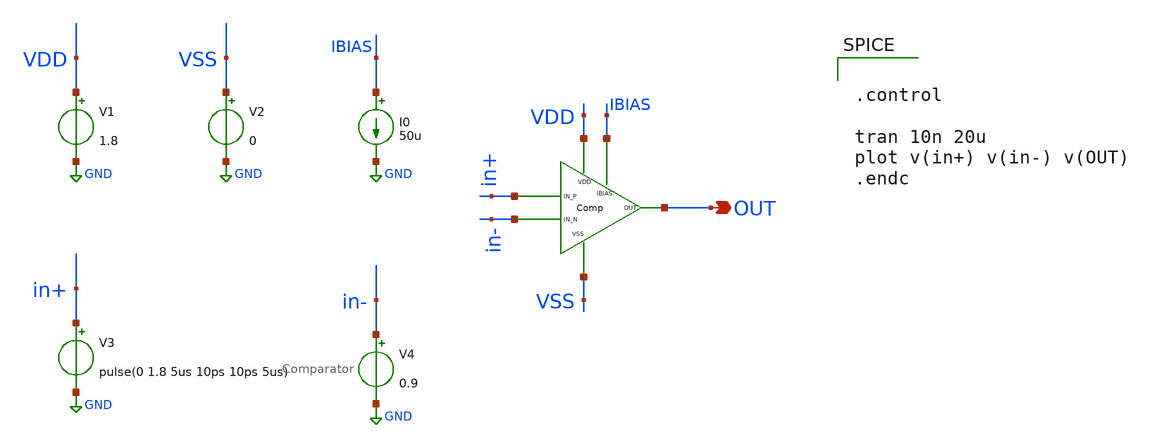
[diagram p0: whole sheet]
** sch_path: xschem/DC_DC_Converter_xschem/OTHERS/DC_DC_Converter_V7/Comparator/Comparator_TB.sch
**.subckt Comparator_TB OUT
*.opin OUT
V1 VDD GND 1.8
V2 VSS GND 0
V3 in+ GND pulse(0 1.8 5us 10ps 10ps 5us)
V4 in- GND 0.9
I0 IBIAS GND 50u
XM1 IBIAS VDD in+ in- VSS OUT Comparator
**** begin user architecture code


.control

tran 10n 20u
plot v(in+) v(in-) v(OUT)
.endc



** opencircuitdesign pdks install
.lib $::SKYWATER_MODELS/sky130.lib.spice tt


**** end user architecture code
**.ends

* expanding   symbol:  DC_DC_Converter/Comparator/Comparator.sym # of pins=6
** sym_path: xschem/DC_DC_Converter_xschem/OTHERS/DC_DC_Converter_V7/Comparator/Comparator.sym
** sch_path: xschem/DC_DC_Converter_xschem/OTHERS/DC_DC_Converter_V7/Comparator/Comparator.sch
.subckt Comparator IBIAS VDD IN_P IN_N VSS OUT
*.iopin VDD
*.iopin VSS
*.iopin IN_P
*.iopin IN_N
*.iopin OUT
*.iopin IBIAS
XM15 1_N IN_P IBIAS VSS sky130_fd_pr__nfet_01v8 L=1 W=5 nf=1 ad='int((nf+1)/2) * W/nf * 0.29' as='int((nf+2)/2) * W/nf * 0.29'
+ pd='2*int((nf+1)/2) * (W/nf + 0.29)' ps='2*int((nf+2)/2) * (W/nf + 0.29)' nrd='0.29 / W' nrs='0.29 / W'
+ sa=0 sb=0 sd=0 mult=1 m=1
XM1 1_P IN_N IBIAS VSS sky130_fd_pr__nfet_01v8 L=1 W=5 nf=1 ad='int((nf+1)/2) * W/nf * 0.29' as='int((nf+2)/2) * W/nf * 0.29'
+ pd='2*int((nf+1)/2) * (W/nf + 0.29)' ps='2*int((nf+2)/2) * (W/nf + 0.29)' nrd='0.29 / W' nrs='0.29 / W'
+ sa=0 sb=0 sd=0 mult=1 m=1
XM2 2_P 2_P VSS VSS sky130_fd_pr__nfet_01v8 L=2 W=2 nf=1 ad='int((nf+1)/2) * W/nf * 0.29' as='int((nf+2)/2) * W/nf * 0.29'
+ pd='2*int((nf+1)/2) * (W/nf + 0.29)' ps='2*int((nf+2)/2) * (W/nf + 0.29)' nrd='0.29 / W' nrs='0.29 / W'
+ sa=0 sb=0 sd=0 mult=1 m=1
XM10 2_N 2_P VSS VSS sky130_fd_pr__nfet_01v8 L=2 W=2 nf=1 ad='int((nf+1)/2) * W/nf * 0.29' as='int((nf+2)/2) * W/nf * 0.29'
+ pd='2*int((nf+1)/2) * (W/nf + 0.29)' ps='2*int((nf+2)/2) * (W/nf + 0.29)' nrd='0.29 / W' nrs='0.29 / W'
+ sa=0 sb=0 sd=0 mult=1 m=1
XM11 OP_1 2_N VSS VSS sky130_fd_pr__nfet_01v8 L=1 W=1 nf=1 ad='int((nf+1)/2) * W/nf * 0.29' as='int((nf+2)/2) * W/nf * 0.29'
+ pd='2*int((nf+1)/2) * (W/nf + 0.29)' ps='2*int((nf+2)/2) * (W/nf + 0.29)' nrd='0.29 / W' nrs='0.29 / W'
+ sa=0 sb=0 sd=0 mult=1 m=1
XM13 OUT OP_1 VSS VSS sky130_fd_pr__nfet_01v8 L=1 W=1 nf=1 ad='int((nf+1)/2) * W/nf * 0.29' as='int((nf+2)/2) * W/nf * 0.29'
+ pd='2*int((nf+1)/2) * (W/nf + 0.29)' ps='2*int((nf+2)/2) * (W/nf + 0.29)' nrd='0.29 / W' nrs='0.29 / W'
+ sa=0 sb=0 sd=0 mult=1 m=1
XM9 2_P 1_N VDD VDD sky130_fd_pr__pfet_01v8 L=0.5 W=1 nf=1 ad='int((nf+1)/2) * W/nf * 0.29' as='int((nf+2)/2) * W/nf * 0.29'
+ pd='2*int((nf+1)/2) * (W/nf + 0.29)' ps='2*int((nf+2)/2) * (W/nf + 0.29)' nrd='0.29 / W' nrs='0.29 / W'
+ sa=0 sb=0 sd=0 mult=1 m=1
XM6 1_N 1_N VDD VDD sky130_fd_pr__pfet_01v8 L=0.5 W=1.5 nf=1 ad='int((nf+1)/2) * W/nf * 0.29' as='int((nf+2)/2) * W/nf * 0.29'
+ pd='2*int((nf+1)/2) * (W/nf + 0.29)' ps='2*int((nf+2)/2) * (W/nf + 0.29)' nrd='0.29 / W' nrs='0.29 / W'
+ sa=0 sb=0 sd=0 mult=1 m=1
XM4 1_N 1_P VDD VDD sky130_fd_pr__pfet_01v8 L=0.5 W=1.5 nf=1 ad='int((nf+1)/2) * W/nf * 0.29' as='int((nf+2)/2) * W/nf * 0.29'
+ pd='2*int((nf+1)/2) * (W/nf + 0.29)' ps='2*int((nf+2)/2) * (W/nf + 0.29)' nrd='0.29 / W' nrs='0.29 / W'
+ sa=0 sb=0 sd=0 mult=1 m=1
XM3 1_P 1_N VDD VDD sky130_fd_pr__pfet_01v8 L=0.5 W=1.5 nf=1 ad='int((nf+1)/2) * W/nf * 0.29' as='int((nf+2)/2) * W/nf * 0.29'
+ pd='2*int((nf+1)/2) * (W/nf + 0.29)' ps='2*int((nf+2)/2) * (W/nf + 0.29)' nrd='0.29 / W' nrs='0.29 / W'
+ sa=0 sb=0 sd=0 mult=1 m=1
XM5 1_P 1_P VDD VDD sky130_fd_pr__pfet_01v8 L=0.5 W=1.5 nf=1 ad='int((nf+1)/2) * W/nf * 0.29' as='int((nf+2)/2) * W/nf * 0.29'
+ pd='2*int((nf+1)/2) * (W/nf + 0.29)' ps='2*int((nf+2)/2) * (W/nf + 0.29)' nrd='0.29 / W' nrs='0.29 / W'
+ sa=0 sb=0 sd=0 mult=1 m=1
XM7 2_N 1_P VDD VDD sky130_fd_pr__pfet_01v8 L=0.5 W=1 nf=1 ad='int((nf+1)/2) * W/nf * 0.29' as='int((nf+2)/2) * W/nf * 0.29'
+ pd='2*int((nf+1)/2) * (W/nf + 0.29)' ps='2*int((nf+2)/2) * (W/nf + 0.29)' nrd='0.29 / W' nrs='0.29 / W'
+ sa=0 sb=0 sd=0 mult=1 m=1
XM8 OP_1 2_N VDD VDD sky130_fd_pr__pfet_01v8 L=1 W=2.5 nf=1 ad='int((nf+1)/2) * W/nf * 0.29' as='int((nf+2)/2) * W/nf * 0.29'
+ pd='2*int((nf+1)/2) * (W/nf + 0.29)' ps='2*int((nf+2)/2) * (W/nf + 0.29)' nrd='0.29 / W' nrs='0.29 / W'
+ sa=0 sb=0 sd=0 mult=1 m=1
XM12 OUT OP_1 VDD VDD sky130_fd_pr__pfet_01v8 L=1 W=2.5 nf=1 ad='int((nf+1)/2) * W/nf * 0.29' as='int((nf+2)/2) * W/nf * 0.29'
+ pd='2*int((nf+1)/2) * (W/nf + 0.29)' ps='2*int((nf+2)/2) * (W/nf + 0.29)' nrd='0.29 / W' nrs='0.29 / W'
+ sa=0 sb=0 sd=0 mult=1 m=1
.ends

.GLOBAL GND
.end
